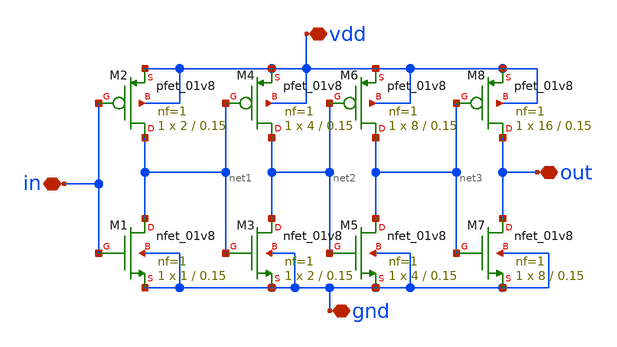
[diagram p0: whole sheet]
** sch_path: buffer_sky130.sch
**.subckt buffer_sky130 vdd gnd in out
*.iopin vdd
*.iopin gnd
*.iopin in
*.iopin out
XM1 net1 in gnd gnd sky130_fd_pr__nfet_01v8 L=0.15 W=1 nf=1 ad='int((1 + 1)/2) * 1 / 1 * 0.29' as='int((1 + 2)/2) * 1 / 1 * 0.29'
+ pd='2*int((1 + 1)/2) * (1 / 1 + 0.29)' ps='2*int((1 + 2)/2) * (1 / 1 + 0.29)' nrd='0.29 / 1 ' nrs='0.29 / 1 '
+ sa=0 sb=0 sd=0 mult=1 m=1
XM2 net1 in vdd vdd sky130_fd_pr__pfet_01v8 L=0.15 W=2 nf=1 ad='int((1 + 1)/2) * 2 / 1 * 0.29' as='int((1 + 2)/2) * 2 / 1 * 0.29'
+ pd='2*int((1 + 1)/2) * (2 / 1 + 0.29)' ps='2*int((1 + 2)/2) * (2 / 1 + 0.29)' nrd='0.29 / 2 ' nrs='0.29 / 2 '
+ sa=0 sb=0 sd=0 mult=1 m=1
XM3 net2 net1 gnd gnd sky130_fd_pr__nfet_01v8 L=0.15 W=2 nf=1 ad='int((1 + 1)/2) * 2 / 1 * 0.29' as='int((1 + 2)/2) * 2 / 1 * 0.29'
+ pd='2*int((1 + 1)/2) * (2 / 1 + 0.29)' ps='2*int((1 + 2)/2) * (2 / 1 + 0.29)' nrd='0.29 / 2 ' nrs='0.29 / 2 '
+ sa=0 sb=0 sd=0 mult=1 m=1
XM4 net2 net1 vdd vdd sky130_fd_pr__pfet_01v8 L=0.15 W=4 nf=1 ad='int((1 + 1)/2) * 4 / 1 * 0.29' as='int((1 + 2)/2) * 4 / 1 * 0.29'
+ pd='2*int((1 + 1)/2) * (4 / 1 + 0.29)' ps='2*int((1 + 2)/2) * (4 / 1 + 0.29)' nrd='0.29 / 4 ' nrs='0.29 / 4 '
+ sa=0 sb=0 sd=0 mult=1 m=1
XM5 net3 net2 gnd gnd sky130_fd_pr__nfet_01v8 L=0.15 W=4 nf=1 ad='int((1 + 1)/2) * 4 / 1 * 0.29' as='int((1 + 2)/2) * 4 / 1 * 0.29'
+ pd='2*int((1 + 1)/2) * (4 / 1 + 0.29)' ps='2*int((1 + 2)/2) * (4 / 1 + 0.29)' nrd='0.29 / 4 ' nrs='0.29 / 4 '
+ sa=0 sb=0 sd=0 mult=1 m=1
XM6 net3 net2 vdd vdd sky130_fd_pr__pfet_01v8 L=0.15 W=8 nf=1 ad='int((1 + 1)/2) * 8 / 1 * 0.29' as='int((1 + 2)/2) * 8 / 1 * 0.29'
+ pd='2*int((1 + 1)/2) * (8 / 1 + 0.29)' ps='2*int((1 + 2)/2) * (8 / 1 + 0.29)' nrd='0.29 / 8 ' nrs='0.29 / 8 '
+ sa=0 sb=0 sd=0 mult=1 m=1
XM7 out net3 gnd gnd sky130_fd_pr__nfet_01v8 L=0.15 W=8 nf=1 ad='int((1 + 1)/2) * 8 / 1 * 0.29' as='int((1 + 2)/2) * 8 / 1 * 0.29'
+ pd='2*int((1 + 1)/2) * (8 / 1 + 0.29)' ps='2*int((1 + 2)/2) * (8 / 1 + 0.29)' nrd='0.29 / 8 ' nrs='0.29 / 8 '
+ sa=0 sb=0 sd=0 mult=1 m=1
XM8 out net3 vdd vdd sky130_fd_pr__pfet_01v8 L=0.15 W=16 nf=1 ad='int((1 + 1)/2) * 16 / 1 * 0.29' as='int((1 + 2)/2) * 16 / 1 * 0.29'
+ pd='2*int((1 + 1)/2) * (16 / 1 + 0.29)' ps='2*int((1 + 2)/2) * (16 / 1 + 0.29)' nrd='0.29 / 16 ' nrs='0.29 / 16 '
+ sa=0 sb=0 sd=0 mult=1 m=1
**.ends
.end
